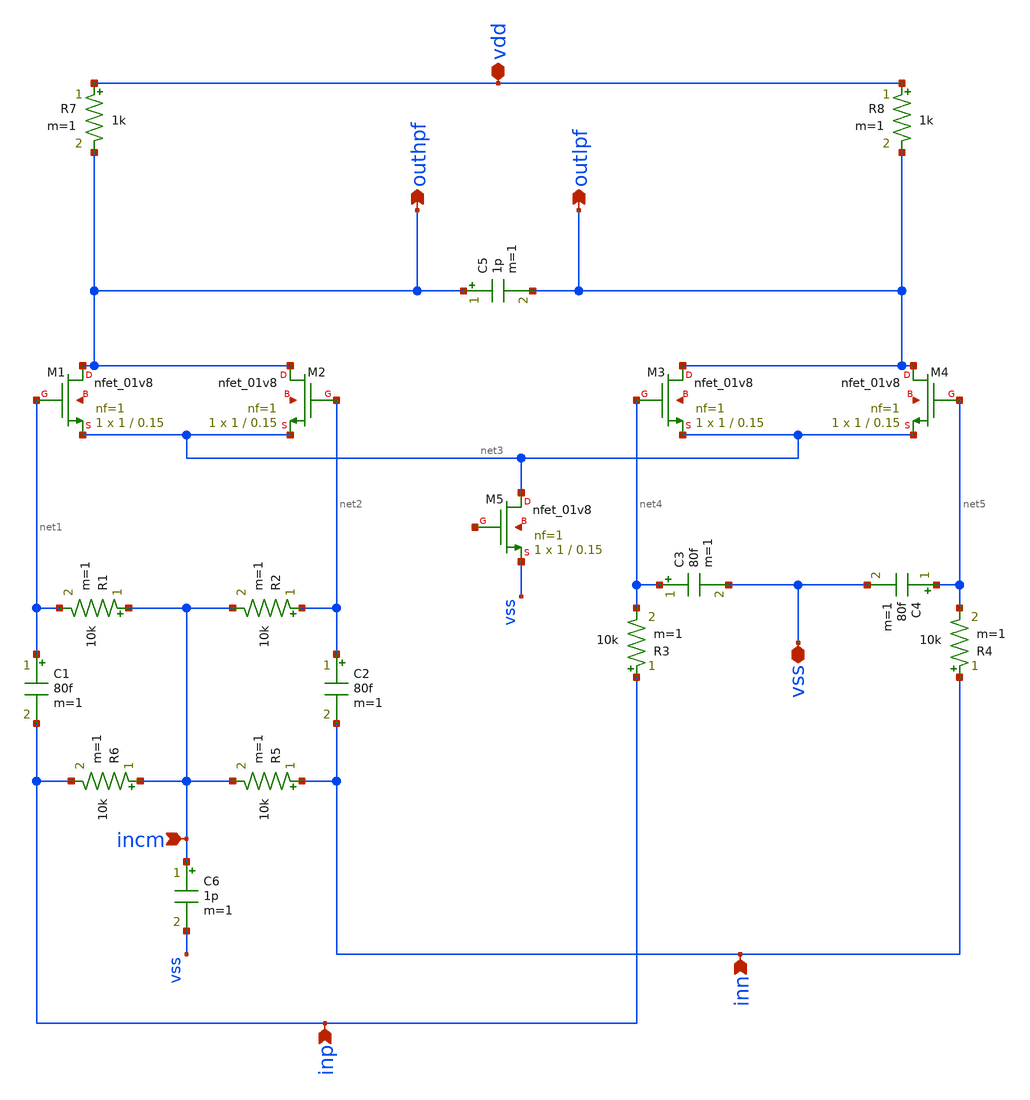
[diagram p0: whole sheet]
** sch_path: CTLE/power_detector.sch
**.subckt power_detector vdd vss inp inn incm outhpf outlpf
*.iopin vdd
*.iopin vss
*.ipin inp
*.ipin inn
*.ipin incm
*.opin outhpf
*.opin outlpf
R1 incm net1 10k m=1
R2 net2 incm 10k m=1
R3 inp net4 10k m=1
R4 inn net5 10k m=1
C1 net1 inp 80f m=1
C2 net2 inn 80f m=1
R5 inn incm 10k m=1
R6 incm inp 10k m=1
C3 net4 vss 80f m=1
C4 net5 vss 80f m=1
XM1 outhpf net1 net3 net6 sky130_fd_pr__nfet_01v8 L=0.15 W=1 nf=1 ad='int((nf+1)/2) * W/nf * 0.29' as='int((nf+2)/2) * W/nf * 0.29'
+ pd='2*int((nf+1)/2) * (W/nf + 0.29)' ps='2*int((nf+2)/2) * (W/nf + 0.29)' nrd='0.29 / W' nrs='0.29 / W'
+ sa=0 sb=0 sd=0 mult=1 m=1
XM2 outhpf net2 net3 net7 sky130_fd_pr__nfet_01v8 L=0.15 W=1 nf=1 ad='int((nf+1)/2) * W/nf * 0.29' as='int((nf+2)/2) * W/nf * 0.29'
+ pd='2*int((nf+1)/2) * (W/nf + 0.29)' ps='2*int((nf+2)/2) * (W/nf + 0.29)' nrd='0.29 / W' nrs='0.29 / W'
+ sa=0 sb=0 sd=0 mult=1 m=1
XM3 outlpf net4 net3 net8 sky130_fd_pr__nfet_01v8 L=0.15 W=1 nf=1 ad='int((nf+1)/2) * W/nf * 0.29' as='int((nf+2)/2) * W/nf * 0.29'
+ pd='2*int((nf+1)/2) * (W/nf + 0.29)' ps='2*int((nf+2)/2) * (W/nf + 0.29)' nrd='0.29 / W' nrs='0.29 / W'
+ sa=0 sb=0 sd=0 mult=1 m=1
XM4 outlpf net5 net3 net9 sky130_fd_pr__nfet_01v8 L=0.15 W=1 nf=1 ad='int((nf+1)/2) * W/nf * 0.29' as='int((nf+2)/2) * W/nf * 0.29'
+ pd='2*int((nf+1)/2) * (W/nf + 0.29)' ps='2*int((nf+2)/2) * (W/nf + 0.29)' nrd='0.29 / W' nrs='0.29 / W'
+ sa=0 sb=0 sd=0 mult=1 m=1
C5 outhpf outlpf 1p m=1
XM5 net3 net10 vss net11 sky130_fd_pr__nfet_01v8 L=0.15 W=1 nf=1 ad='int((nf+1)/2) * W/nf * 0.29' as='int((nf+2)/2) * W/nf * 0.29'
+ pd='2*int((nf+1)/2) * (W/nf + 0.29)' ps='2*int((nf+2)/2) * (W/nf + 0.29)' nrd='0.29 / W' nrs='0.29 / W'
+ sa=0 sb=0 sd=0 mult=1 m=1
R7 vdd outhpf 1k m=1
R8 vdd outlpf 1k m=1
C6 incm vss 1p m=1
**.ends
.end
